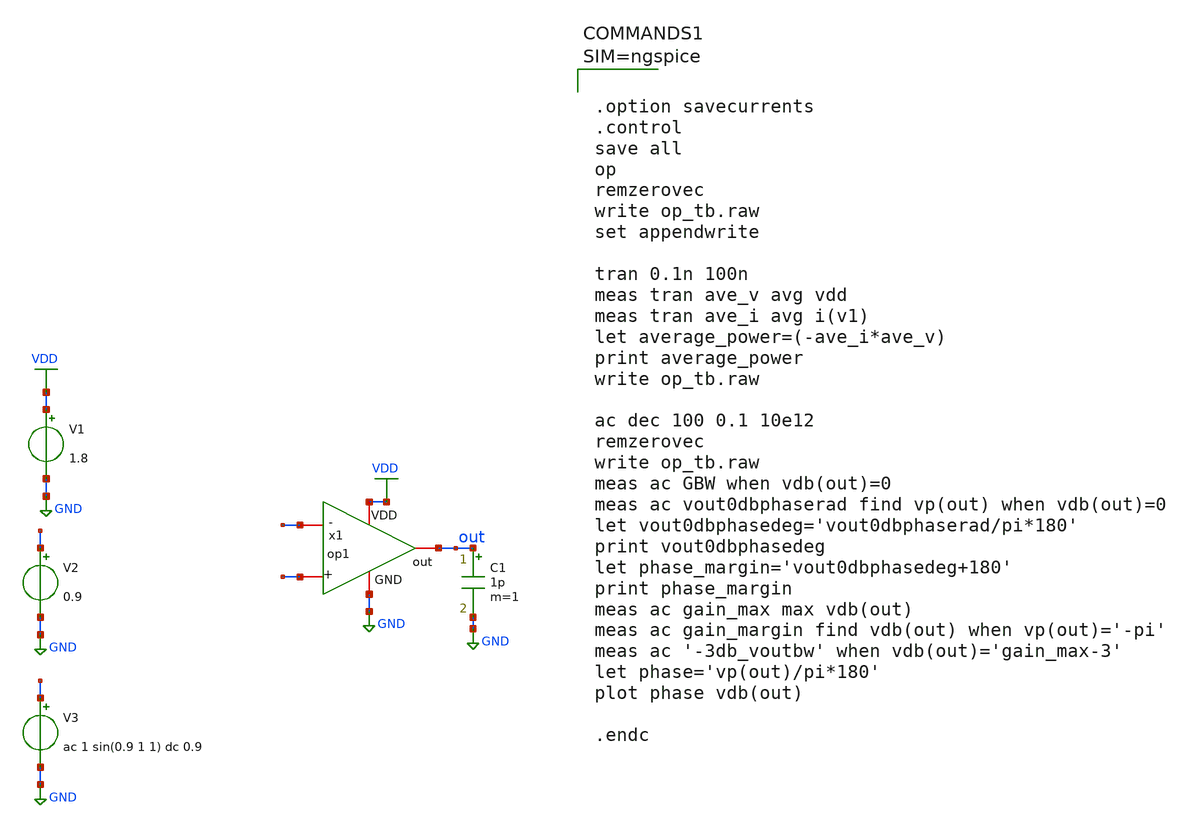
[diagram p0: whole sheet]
** sch_path: xschem/op1_tb.sch
**.subckt op1_tb
V1 VDD GND 1.8
V2 - GND 0.9
V3 + GND ac 1 sin(0.9 1 1) dc 0.9
x1 VDD out - + GND op1
C1 out GND 1p m=1
**** begin user architecture code

** opencircuitdesign pdks install
.lib $::SKYWATER_MODELS/sky130.lib.spice tt





.option savecurrents
.control
save all
op
remzerovec
write op_tb.raw
set appendwrite

tran 0.1n 100n
meas tran ave_v avg vdd
meas tran ave_i avg i(v1)
let average_power=(-ave_i*ave_v)
print average_power
write op_tb.raw

ac dec 100 0.1 10e12
remzerovec
write op_tb.raw
meas ac GBW when vdb(out)=0
meas ac vout0dbphaserad find vp(out) when vdb(out)=0
let vout0dbphasedeg='vout0dbphaserad/pi*180'
print vout0dbphasedeg
let phase_margin='vout0dbphasedeg+180'
print phase_margin
meas ac gain_max max vdb(out)
meas ac gain_margin find vdb(out) when vp(out)='-pi'
meas ac '-3db_voutbw' when vdb(out)='gain_max-3'
let phase='vp(out)/pi*180'
plot phase vdb(out)

.endc



**** end user architecture code
**.ends

* expanding   symbol:  op1.sym # of pins=5
** sym_path: xschem/op1.sym
** sch_path: xschem/op1.sch
.subckt op1 VDD out - + GND
*.iopin VDD
*.iopin GND
*.iopin -
*.iopin +
*.iopin out
**** begin user architecture code


.param L=20
.param W=1


**** end user architecture code
C2 out net5 2.2p m=1
R2 net5 net1 850k m=1
XM1 bias bias GND GND sky130_fd_pr__nfet_01v8 L={L} W={W/1.5} nf=1 ad='int((nf+1)/2) * W/nf * 0.29' as='int((nf+2)/2) * W/nf * 0.29'
+ pd='2*int((nf+1)/2) * (W/nf + 0.29)' ps='2*int((nf+2)/2) * (W/nf + 0.29)' nrd='0.29 / W' nrs='0.29 / W'
+ sa=0 sb=0 sd=0 mult=2 m=2
XM2 net4 bias GND GND sky130_fd_pr__nfet_01v8 L={L} W={W/1.5} nf=1 ad='int((nf+1)/2) * W/nf * 0.29' as='int((nf+2)/2) * W/nf * 0.29'
+ pd='2*int((nf+1)/2) * (W/nf + 0.29)' ps='2*int((nf+2)/2) * (W/nf + 0.29)' nrd='0.29 / W' nrs='0.29 / W'
+ sa=0 sb=0 sd=0 mult=2 m=2
XM3 net2 - net3 GND sky130_fd_pr__nfet_01v8 L={L} W={W} nf=1 ad='int((nf+1)/2) * W/nf * 0.29' as='int((nf+2)/2) * W/nf * 0.29'
+ pd='2*int((nf+1)/2) * (W/nf + 0.29)' ps='2*int((nf+2)/2) * (W/nf + 0.29)' nrd='0.29 / W' nrs='0.29 / W'
+ sa=0 sb=0 sd=0 mult=4 m=4
XM4 net1 + net3 GND sky130_fd_pr__nfet_01v8 L={L} W={W} nf=1 ad='int((nf+1)/2) * W/nf * 0.29' as='int((nf+2)/2) * W/nf * 0.29'
+ pd='2*int((nf+1)/2) * (W/nf + 0.29)' ps='2*int((nf+2)/2) * (W/nf + 0.29)' nrd='0.29 / W' nrs='0.29 / W'
+ sa=0 sb=0 sd=0 mult=4 m=4
XM6 bias net4 VDD VDD sky130_fd_pr__pfet_01v8 L={L} W={W/1.5} nf=1 ad='int((nf+1)/2) * W/nf * 0.29' as='int((nf+2)/2) * W/nf * 0.29'
+ pd='2*int((nf+1)/2) * (W/nf + 0.29)' ps='2*int((nf+2)/2) * (W/nf + 0.29)' nrd='0.29 / W' nrs='0.29 / W'
+ sa=0 sb=0 sd=0 mult=2 m=2
XM7 net4 net4 VDD VDD sky130_fd_pr__pfet_01v8 L={L} W={W/1.5} nf=1 ad='int((nf+1)/2) * W/nf * 0.29' as='int((nf+2)/2) * W/nf * 0.29'
+ pd='2*int((nf+1)/2) * (W/nf + 0.29)' ps='2*int((nf+2)/2) * (W/nf + 0.29)' nrd='0.29 / W' nrs='0.29 / W'
+ sa=0 sb=0 sd=0 mult=2 m=2
XM8 net1 net2 VDD VDD sky130_fd_pr__pfet_01v8 L={L} W={W} nf=1 ad='int((nf+1)/2) * W/nf * 0.29' as='int((nf+2)/2) * W/nf * 0.29'
+ pd='2*int((nf+1)/2) * (W/nf + 0.29)' ps='2*int((nf+2)/2) * (W/nf + 0.29)' nrd='0.29 / W' nrs='0.29 / W'
+ sa=0 sb=0 sd=0 mult=4 m=4
XM9 net2 net2 VDD VDD sky130_fd_pr__pfet_01v8 L={L} W={W} nf=1 ad='int((nf+1)/2) * W/nf * 0.29' as='int((nf+2)/2) * W/nf * 0.29'
+ pd='2*int((nf+1)/2) * (W/nf + 0.29)' ps='2*int((nf+2)/2) * (W/nf + 0.29)' nrd='0.29 / W' nrs='0.29 / W'
+ sa=0 sb=0 sd=0 mult=4 m=4
XM5 net3 bias GND GND sky130_fd_pr__nfet_01v8 L={L} W={W} nf=1 ad='int((nf+1)/2) * W/nf * 0.29' as='int((nf+2)/2) * W/nf * 0.29'
+ pd='2*int((nf+1)/2) * (W/nf + 0.29)' ps='2*int((nf+2)/2) * (W/nf + 0.29)' nrd='0.29 / W' nrs='0.29 / W'
+ sa=0 sb=0 sd=0 mult=4 m=4
XM10 out net1 VDD VDD sky130_fd_pr__pfet_01v8 L={L} W={W*1.1} nf=1 ad='int((nf+1)/2) * W/nf * 0.29' as='int((nf+2)/2) * W/nf * 0.29'
+ pd='2*int((nf+1)/2) * (W/nf + 0.29)' ps='2*int((nf+2)/2) * (W/nf + 0.29)' nrd='0.29 / W' nrs='0.29 / W'
+ sa=0 sb=0 sd=0 mult=4 m=4
XM11 out bias GND GND sky130_fd_pr__nfet_01v8 L={L} W={W} nf=1 ad='int((nf+1)/2) * W/nf * 0.29' as='int((nf+2)/2) * W/nf * 0.29'
+ pd='2*int((nf+1)/2) * (W/nf + 0.29)' ps='2*int((nf+2)/2) * (W/nf + 0.29)' nrd='0.29 / W' nrs='0.29 / W'
+ sa=0 sb=0 sd=0 mult=2 m=2
.ends

.GLOBAL VDD
.GLOBAL GND
.end
